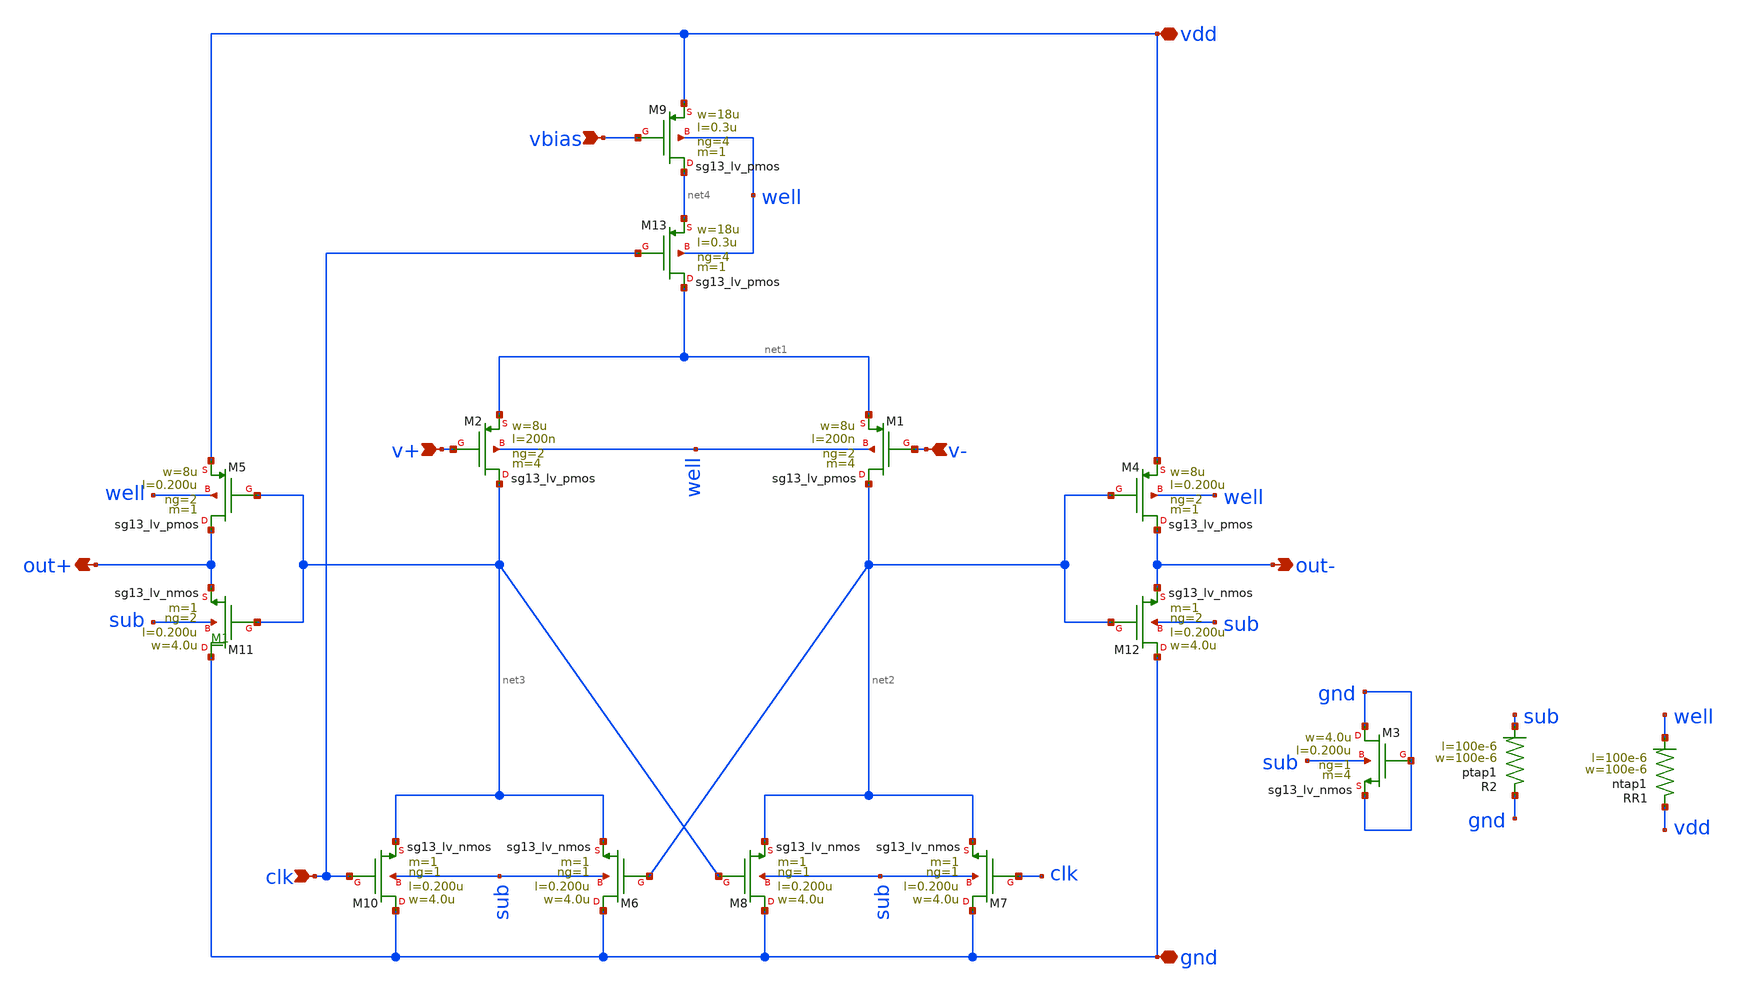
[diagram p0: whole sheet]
** sch_path: modules/module_3_8_bit_SAR_ADC/part_5_layout/comparator/schematic/DIFF_COMPARATOR.sch
**.subckt DIFF_COMPARATOR vdd gnd v+ v- clk out- out+ vbias
*.iopin vdd
*.iopin gnd
*.ipin v+
*.ipin v-
*.ipin clk
*.opin out-
*.opin out+
*.ipin vbias
XM2 net3 v+ net1 well sg13_lv_pmos w=8u l=200n ng=2 m=4 mm_ok=1
XM1 net2 v- net1 well sg13_lv_pmos w=8u l=200n ng=2 m=4 mm_ok=1
XM4 out- net2 vdd well sg13_lv_pmos w=8u l=0.200u ng=2 m=1 mm_ok=1
XM5 out+ net3 vdd well sg13_lv_pmos w=8u l=0.200u ng=2 m=1 mm_ok=1
XM11 gnd net3 out+ sub sg13_lv_nmos w=4.0u l=0.200u ng=2 m=1 mm_ok=1
XM12 gnd net2 out- sub sg13_lv_nmos w=4.0u l=0.200u ng=2 m=1 mm_ok=1
XM6 gnd net2 net3 sub sg13_lv_nmos w=4.0u l=0.200u ng=1 m=1 mm_ok=1
XM10 gnd clk net3 sub sg13_lv_nmos w=4.0u l=0.200u ng=1 m=1 mm_ok=1
XM7 gnd clk net2 sub sg13_lv_nmos w=4.0u l=0.200u ng=1 m=1 mm_ok=1
XM8 gnd net3 net2 sub sg13_lv_nmos w=4.0u l=0.200u ng=1 m=1 mm_ok=1
XR1 vdd well ntap1 R=94.23m w=100e-6 l=100e-6
XM3 gnd gnd gnd sub sg13_lv_nmos w=4.0u l=0.200u ng=1 m=4 mm_ok=1
XR2 gnd sub ptap1 R=94.23m w=100e-6 l=100e-6
XM13 net1 clk net4 well sg13_lv_pmos w=18u l=0.3u ng=4 m=1 mm_ok=1
XM9 net4 vbias vdd well sg13_lv_pmos w=18u l=0.3u ng=4 m=1 mm_ok=1
**.ends
.end
